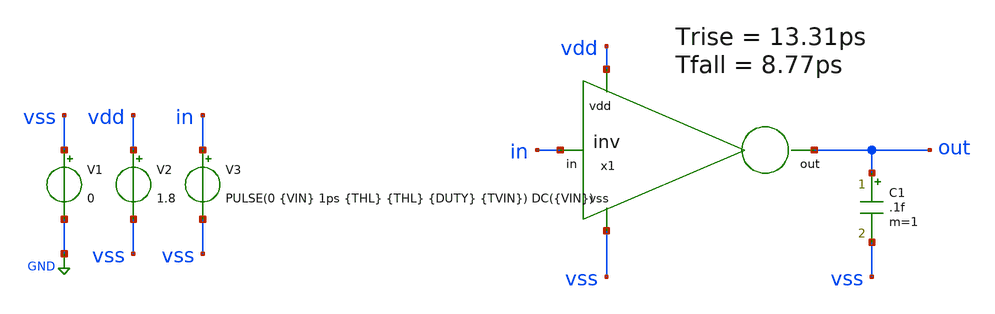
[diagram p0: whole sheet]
** sch_path: eamta2021/sch/inv/tbInv.sch
**.subckt tbInv
x1 vdd in out vss inv
V1 vss GND 0
V2 vdd vss 1.8
V3 in vss PULSE(0 {VIN} 1ps {THL} {THL} {DUTY} {TVIN}) DC({VIN})
C1 out vss .1f m=1
**** begin user architecture code



* parametros
.param VIN=1.8 WN=.450 WP=.90 THL=1p TVIN=100n DUTY=50n
.options TEMP=27.0

* include corners
.lib /home/eamta/skywater/skywater-pdk/libraries/sky130_fd_pr_ngspice/latest/models/corners/sky130.lib TT

* saves
.save all  @M.x1.xm1.msky130_fd_pr__nfet_01v8[id]  @M.x1.xm1.msky130_fd_pr__nfet_01v8[vds]  @M.x1.xm1.msky130_fd_pr__nfet_01v8[vgs]  @M.x1.xm1.msky130_fd_pr__nfet_01v8[vth]  @M.x1.xm2.msky130_fd_pr__pfet_01v8[id]  @M.x1.xm2.msky130_fd_pr__pfet_01v8[vds]  @M.x1.xm2.msky130_fd_pr__pfet_01v8[vgs]  @M.x1.xm2.msky130_fd_pr__pfet_01v8[vth]

* SIM
.control
	******************************************************
	let At=.005ns
	tran 0.005ns 250ns

	setplot tran1
	plot v(out) v(in) .18 1.62 xlimit 50ns 50.05ns
	plot v(out) v(in) .18 1.62 xlimit 100ns 100.05ns
	*plot tran1.@M.x1.xm1.msky130_fd_pr__nfet_01v8[vds]
	*plot tran1.@M.x1.xm1.msky130_fd_pr__nfet_01v8[id] tran1.@M.x1.xm2.msky130_fd_pr__pfet_01v8[id]

	set filetype=ascii
	write simInvTran.raw
	reset
	******************************************************
	*dc V3 0 1.8 0.05
	*setplot dc1
	*plot v(out) v(in)
	*plot @M.x1.xm1.msky130_fd_pr__nfet_01v8[id]
	*plot @M.x1.xm1.msky130_fd_pr__nfet_01v8[vd]

	*set filetype=ascii
	*write simInvDc.raw
	*reset
	******************************************************
	op

	set filetype=ascii
	write simInvOp.raw

***********************************************************
	*analisis cuasi parametrico
	*let actParam=1ps
	*let topParam=100ps
	*let detlaParam=10ps

	*foreach x 1ps 10ps 20ps 30ps 40ps 50ps
	*	alterparam THL=$x
	*	tran .01ns .1us
	*	let actParam=actParam+deltaParam
	*	print $x
	*end

	*plot tran1.out tran2.out tran3.out tran4.out tran5.out tran6.out tran7.out tran8.out tran9.out

	print all
.endc

.end


**** end user architecture code
**.ends

* expanding   symbol:  inv/inv.sym # of pins=4
** sym_path: eamta2021/sch/inv/inv.sym
** sch_path: eamta2021/sch/inv/inv.sch
.subckt inv vdd in out vss
*.ipin vdd
*.ipin vss
*.ipin in
*.opin out
XM1 out in vss vss sky130_fd_pr__nfet_01v8 L=0.15 W={WN} nf=1 ad='int((nf+1)/2) * W/nf * 0.29' as='int((nf+2)/2) * W/nf * 0.29'
+ pd='2*int((nf+1)/2) * (W/nf + 0.29)' ps='2*int((nf+2)/2) * (W/nf + 0.29)' nrd='0.29 / W' nrs='0.29 / W'
+ sa=0 sb=0 sd=0 mult=1 m=1
XM2 out in vdd vdd sky130_fd_pr__pfet_01v8 L=0.15 W={WP} nf=1 ad='int((nf+1)/2) * W/nf * 0.29' as='int((nf+2)/2) * W/nf * 0.29'
+ pd='2*int((nf+1)/2) * (W/nf + 0.29)' ps='2*int((nf+2)/2) * (W/nf + 0.29)' nrd='0.29 / W' nrs='0.29 / W'
+ sa=0 sb=0 sd=0 mult=1 m=1
.ends

.GLOBAL GND
.end
